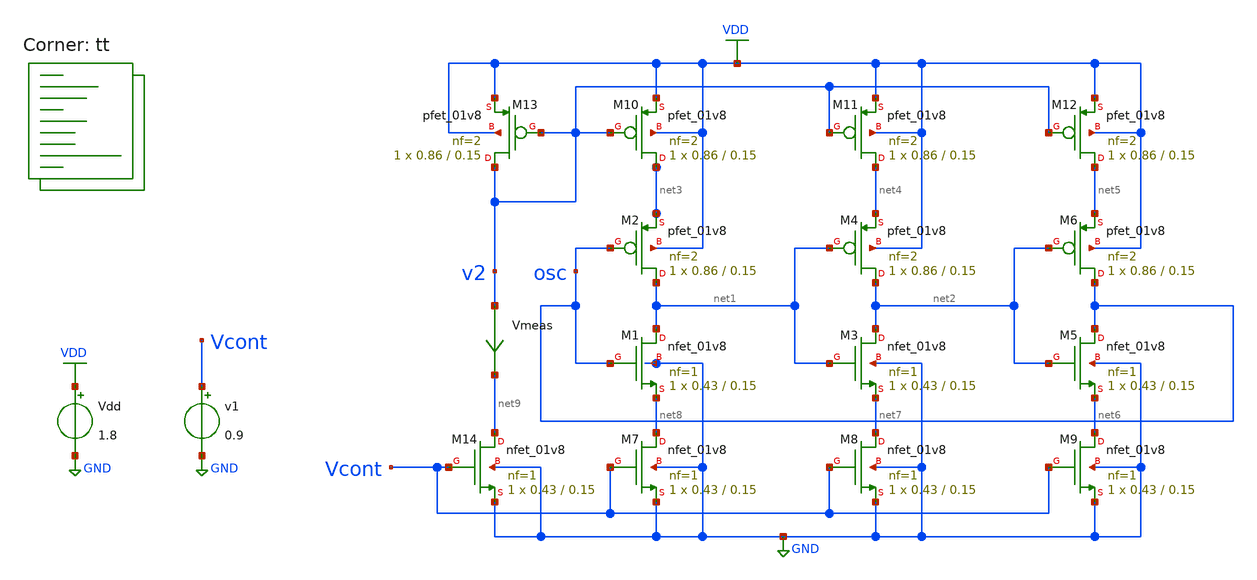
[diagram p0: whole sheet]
** sch_path: projects/pll/vco/xschem_ngspice/tb_current_starved_VCO4.sch
**.subckt tb_current_starved_VCO4
XM1 net1 osc net8 GND sky130_fd_pr__nfet_01v8 L=0.15 W=0.43 nf=1 ad='int((nf+1)/2) * W/nf * 0.29' as='int((nf+2)/2) * W/nf * 0.29'
+ pd='2*int((nf+1)/2) * (W/nf + 0.29)' ps='2*int((nf+2)/2) * (W/nf + 0.29)' nrd='0.29 / W' nrs='0.29 / W'
+ sa=0 sb=0 sd=0 mult=1 m=1
XM2 net1 osc net3 VDD sky130_fd_pr__pfet_01v8 L=0.15 W=0.86 nf=2 ad='int((nf+1)/2) * W/nf * 0.29' as='int((nf+2)/2) * W/nf * 0.29'
+ pd='2*int((nf+1)/2) * (W/nf + 0.29)' ps='2*int((nf+2)/2) * (W/nf + 0.29)' nrd='0.29 / W' nrs='0.29 / W'
+ sa=0 sb=0 sd=0 mult=1 m=1
XM3 net2 net1 net7 GND sky130_fd_pr__nfet_01v8 L=0.15 W=0.43 nf=1 ad='int((nf+1)/2) * W/nf * 0.29' as='int((nf+2)/2) * W/nf * 0.29'
+ pd='2*int((nf+1)/2) * (W/nf + 0.29)' ps='2*int((nf+2)/2) * (W/nf + 0.29)' nrd='0.29 / W' nrs='0.29 / W'
+ sa=0 sb=0 sd=0 mult=1 m=1
XM4 net2 net1 net4 VDD sky130_fd_pr__pfet_01v8 L=0.15 W=0.86 nf=2 ad='int((nf+1)/2) * W/nf * 0.29' as='int((nf+2)/2) * W/nf * 0.29'
+ pd='2*int((nf+1)/2) * (W/nf + 0.29)' ps='2*int((nf+2)/2) * (W/nf + 0.29)' nrd='0.29 / W' nrs='0.29 / W'
+ sa=0 sb=0 sd=0 mult=1 m=1
XM5 osc net2 net6 GND sky130_fd_pr__nfet_01v8 L=0.15 W=0.43 nf=1 ad='int((nf+1)/2) * W/nf * 0.29' as='int((nf+2)/2) * W/nf * 0.29'
+ pd='2*int((nf+1)/2) * (W/nf + 0.29)' ps='2*int((nf+2)/2) * (W/nf + 0.29)' nrd='0.29 / W' nrs='0.29 / W'
+ sa=0 sb=0 sd=0 mult=1 m=1
XM6 osc net2 net5 VDD sky130_fd_pr__pfet_01v8 L=0.15 W=0.86 nf=2 ad='int((nf+1)/2) * W/nf * 0.29' as='int((nf+2)/2) * W/nf * 0.29'
+ pd='2*int((nf+1)/2) * (W/nf + 0.29)' ps='2*int((nf+2)/2) * (W/nf + 0.29)' nrd='0.29 / W' nrs='0.29 / W'
+ sa=0 sb=0 sd=0 mult=1 m=1
XM7 net8 Vcont GND GND sky130_fd_pr__nfet_01v8 L=0.15 W=0.43 nf=1 ad='int((nf+1)/2) * W/nf * 0.29' as='int((nf+2)/2) * W/nf * 0.29'
+ pd='2*int((nf+1)/2) * (W/nf + 0.29)' ps='2*int((nf+2)/2) * (W/nf + 0.29)' nrd='0.29 / W' nrs='0.29 / W'
+ sa=0 sb=0 sd=0 mult=1 m=1
XM8 net7 Vcont GND GND sky130_fd_pr__nfet_01v8 L=0.15 W=0.43 nf=1 ad='int((nf+1)/2) * W/nf * 0.29' as='int((nf+2)/2) * W/nf * 0.29'
+ pd='2*int((nf+1)/2) * (W/nf + 0.29)' ps='2*int((nf+2)/2) * (W/nf + 0.29)' nrd='0.29 / W' nrs='0.29 / W'
+ sa=0 sb=0 sd=0 mult=1 m=1
XM9 net6 Vcont GND GND sky130_fd_pr__nfet_01v8 L=0.15 W=0.43 nf=1 ad='int((nf+1)/2) * W/nf * 0.29' as='int((nf+2)/2) * W/nf * 0.29'
+ pd='2*int((nf+1)/2) * (W/nf + 0.29)' ps='2*int((nf+2)/2) * (W/nf + 0.29)' nrd='0.29 / W' nrs='0.29 / W'
+ sa=0 sb=0 sd=0 mult=1 m=1
XM10 net3 v2 VDD VDD sky130_fd_pr__pfet_01v8 L=0.15 W=0.86 nf=2 ad='int((nf+1)/2) * W/nf * 0.29' as='int((nf+2)/2) * W/nf * 0.29'
+ pd='2*int((nf+1)/2) * (W/nf + 0.29)' ps='2*int((nf+2)/2) * (W/nf + 0.29)' nrd='0.29 / W' nrs='0.29 / W'
+ sa=0 sb=0 sd=0 mult=1 m=1
XM11 net4 v2 VDD VDD sky130_fd_pr__pfet_01v8 L=0.15 W=0.86 nf=2 ad='int((nf+1)/2) * W/nf * 0.29' as='int((nf+2)/2) * W/nf * 0.29'
+ pd='2*int((nf+1)/2) * (W/nf + 0.29)' ps='2*int((nf+2)/2) * (W/nf + 0.29)' nrd='0.29 / W' nrs='0.29 / W'
+ sa=0 sb=0 sd=0 mult=1 m=1
XM12 net5 v2 VDD VDD sky130_fd_pr__pfet_01v8 L=0.15 W=0.86 nf=2 ad='int((nf+1)/2) * W/nf * 0.29' as='int((nf+2)/2) * W/nf * 0.29'
+ pd='2*int((nf+1)/2) * (W/nf + 0.29)' ps='2*int((nf+2)/2) * (W/nf + 0.29)' nrd='0.29 / W' nrs='0.29 / W'
+ sa=0 sb=0 sd=0 mult=1 m=1
Vdd VDD GND 1.8
v1 Vcont GND 0.9
XM13 v2 v2 VDD VDD sky130_fd_pr__pfet_01v8 L=0.15 W=0.86 nf=2 ad='int((nf+1)/2) * W/nf * 0.29' as='int((nf+2)/2) * W/nf * 0.29'
+ pd='2*int((nf+1)/2) * (W/nf + 0.29)' ps='2*int((nf+2)/2) * (W/nf + 0.29)' nrd='0.29 / W' nrs='0.29 / W'
+ sa=0 sb=0 sd=0 mult=1 m=1
XM14 net9 Vcont GND GND sky130_fd_pr__nfet_01v8 L=0.15 W=0.43 nf=1 ad='int((nf+1)/2) * W/nf * 0.29' as='int((nf+2)/2) * W/nf * 0.29'
+ pd='2*int((nf+1)/2) * (W/nf + 0.29)' ps='2*int((nf+2)/2) * (W/nf + 0.29)' nrd='0.29 / W' nrs='0.29 / W'
+ sa=0 sb=0 sd=0 mult=1 m=1
Vmeas v2 net9 0
.save i(vmeas)
**** begin user architecture code
.lib $::SKYWATER_MODELS/sky130.lib.spice tt



.option method=gear
.option wnflag=1

.control
  let v_cont_start = 0.0
  let v_cont_stop = 1.9

  dowhile v_cont_start <= v_cont_stop
    alter v1 $&v_cont_start
    save v(osc) v(vcont) v(v2)
    tran 2ps 30ns
    remzerovec
    write tb_current_starved_VCO4_{$&v_cont_start}.raw
    let filename = v_cont_start * 100
    wrdata /foss/designs/my_design/projects/pll/vco/xschem_ngspice/tb_current_starved_VCO4_{$&filename}.txt
+ v(osc)
    set appendwrite
    reset
    let v_cont_start = v_cont_start + 0.1
  end
.endc



**** end user architecture code
**.ends
.GLOBAL VDD
.GLOBAL GND
.end
